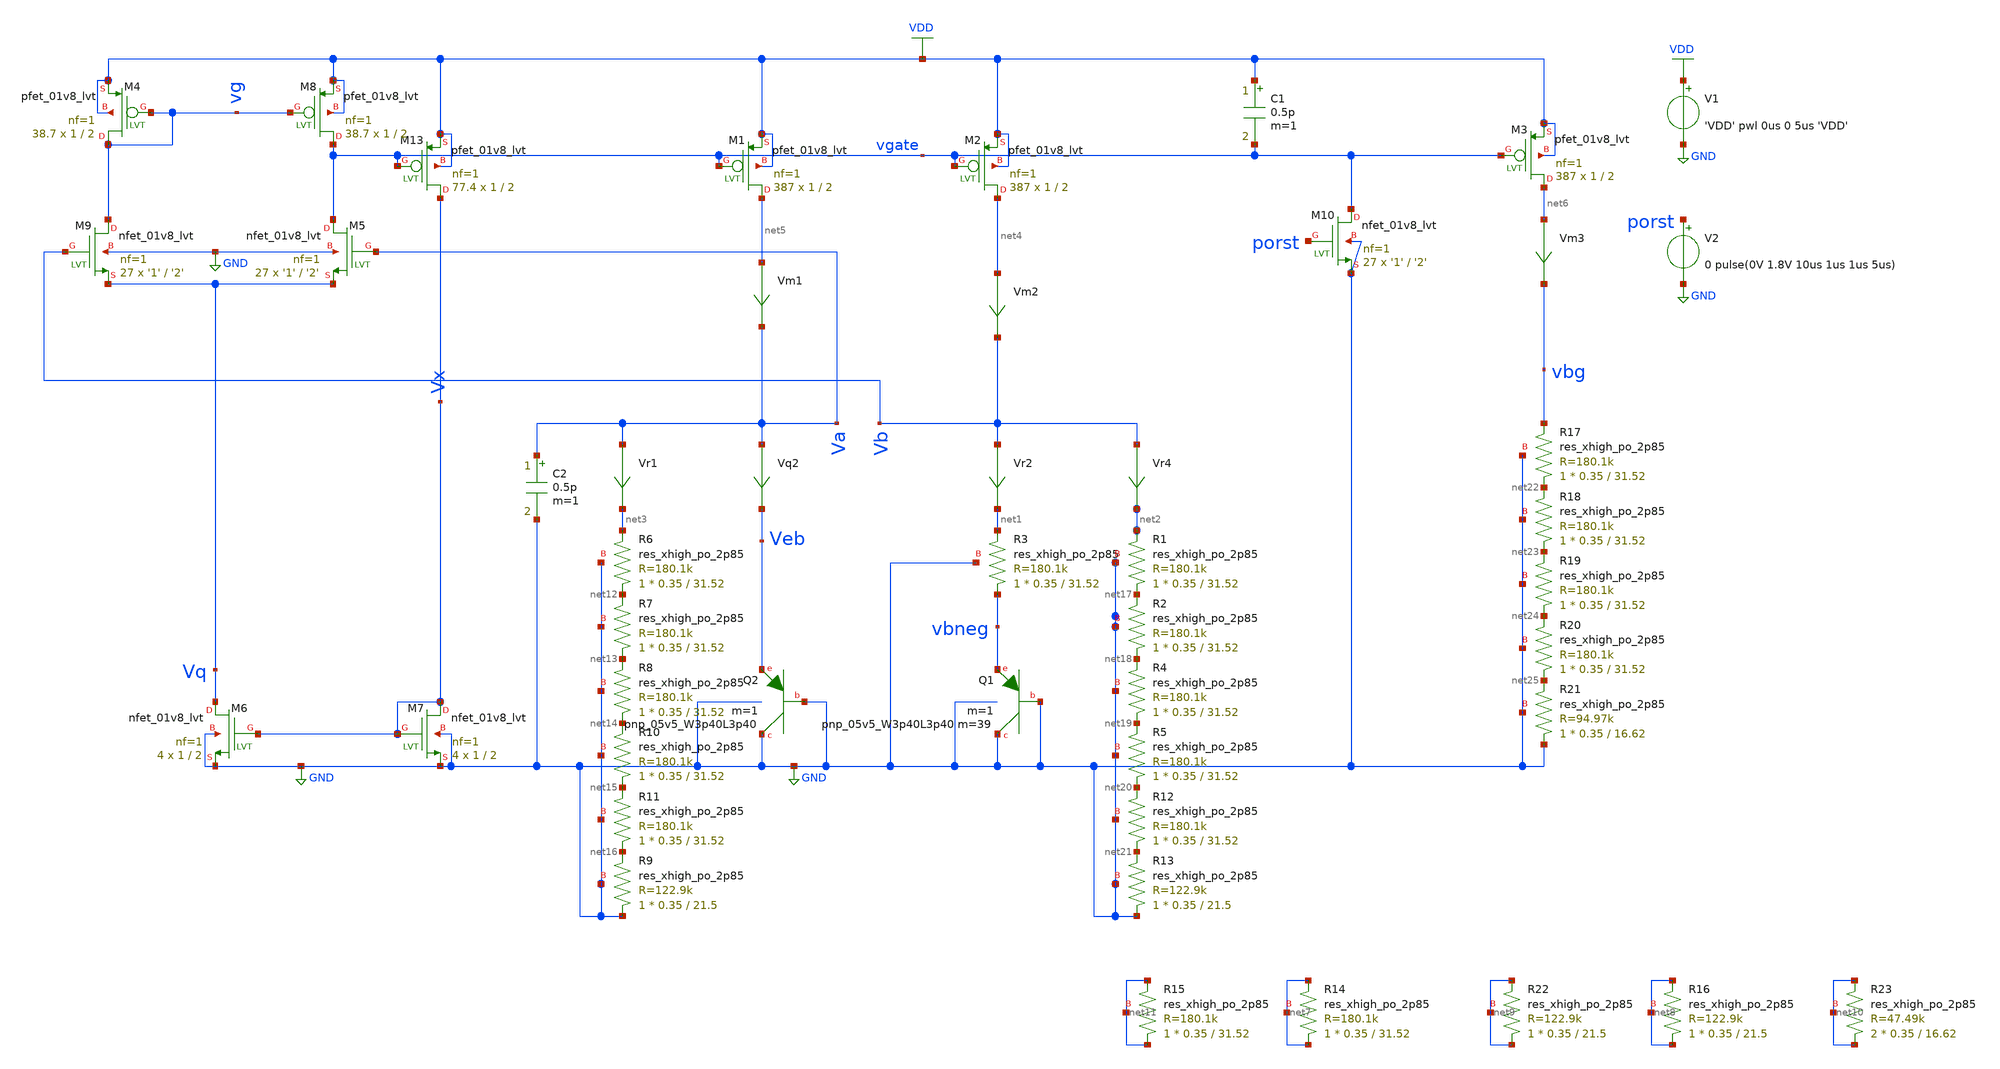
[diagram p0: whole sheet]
** sch_path: schematics/tsmc_bandgap_real_tran_layout.sch
**.subckt tsmc_bandgap_real_tran_layout
V1 VDD GND 'VDD' pwl 0us 0 5us 'VDD'
XQ2 GND GND Veb sky130_fd_pr__pnp_05v5_W3p40L3p40 m=1
Vr4 Vb net2 0
.save i(vr4)
Vr2 Vb net1 0
.save i(vr2)
Vm1 net5 Va 0
.save i(vm1)
Vm2 net4 Vb 0
.save i(vm2)
Vm3 net6 vbg 0
.save i(vm3)
Vr1 Va net3 0
.save i(vr1)
Vq2 Va Veb 0
.save i(vq2)
XQ1 GND GND vbneg sky130_fd_pr__pnp_05v5_W3p40L3p40 m=39 m=1
XM5 vgate Va Vq GND sky130_fd_pr__nfet_01v8_lvt L='2' W='1' nf=1 ad='int((nf+1)/2) * W/nf * 0.29' as='int((nf+2)/2) * W/nf * 0.29'
+ pd='2*int((nf+1)/2) * (W/nf + 0.29)' ps='2*int((nf+2)/2) * (W/nf + 0.29)' nrd='0.29 / W' nrs='0.29 / W'
+ sa=0 sb=0 sd=0 mult=27 m=27
XM6 Vq Vx GND GND sky130_fd_pr__nfet_01v8_lvt L=2 W=1 nf=1 ad='int((nf+1)/2) * W/nf * 0.29' as='int((nf+2)/2) * W/nf * 0.29'
+ pd='2*int((nf+1)/2) * (W/nf + 0.29)' ps='2*int((nf+2)/2) * (W/nf + 0.29)' nrd='0.29 / W' nrs='0.29 / W'
+ sa=0 sb=0 sd=0 mult=4 m=4
XM9 vg Vb Vq GND sky130_fd_pr__nfet_01v8_lvt L='2' W='1' nf=1 ad='int((nf+1)/2) * W/nf * 0.29' as='int((nf+2)/2) * W/nf * 0.29'
+ pd='2*int((nf+1)/2) * (W/nf + 0.29)' ps='2*int((nf+2)/2) * (W/nf + 0.29)' nrd='0.29 / W' nrs='0.29 / W'
+ sa=0 sb=0 sd=0 mult=27 m=27
XM7 Vx Vx GND GND sky130_fd_pr__nfet_01v8_lvt L=2 W=1 nf=1 ad='int((nf+1)/2) * W/nf * 0.29' as='int((nf+2)/2) * W/nf * 0.29'
+ pd='2*int((nf+1)/2) * (W/nf + 0.29)' ps='2*int((nf+2)/2) * (W/nf + 0.29)' nrd='0.29 / W' nrs='0.29 / W'
+ sa=0 sb=0 sd=0 mult=4 m=4
XM13 Vx vgate VDD VDD sky130_fd_pr__pfet_01v8_lvt L=2 W=1 nf=1 ad='int((nf+1)/2) * W/nf * 0.29' as='int((nf+2)/2) * W/nf * 0.29'
+ pd='2*int((nf+1)/2) * (W/nf + 0.29)' ps='2*int((nf+2)/2) * (W/nf + 0.29)' nrd='0.29 / W' nrs='0.29 / W'
+ sa=0 sb=0 sd=0 mult=77.4 m=77.4
XM1 net5 vgate VDD VDD sky130_fd_pr__pfet_01v8_lvt L=2 W=1 nf=1 ad='int((nf+1)/2) * W/nf * 0.29' as='int((nf+2)/2) * W/nf * 0.29'
+ pd='2*int((nf+1)/2) * (W/nf + 0.29)' ps='2*int((nf+2)/2) * (W/nf + 0.29)' nrd='0.29 / W' nrs='0.29 / W'
+ sa=0 sb=0 sd=0 mult=387 m=387
XM2 net4 vgate VDD VDD sky130_fd_pr__pfet_01v8_lvt L=2 W=1 nf=1 ad='int((nf+1)/2) * W/nf * 0.29' as='int((nf+2)/2) * W/nf * 0.29'
+ pd='2*int((nf+1)/2) * (W/nf + 0.29)' ps='2*int((nf+2)/2) * (W/nf + 0.29)' nrd='0.29 / W' nrs='0.29 / W'
+ sa=0 sb=0 sd=0 mult=387 m=387
XM3 net6 vgate VDD VDD sky130_fd_pr__pfet_01v8_lvt L=2 W=1 nf=1 ad='int((nf+1)/2) * W/nf * 0.29' as='int((nf+2)/2) * W/nf * 0.29'
+ pd='2*int((nf+1)/2) * (W/nf + 0.29)' ps='2*int((nf+2)/2) * (W/nf + 0.29)' nrd='0.29 / W' nrs='0.29 / W'
+ sa=0 sb=0 sd=0 mult=387 m=387
XM4 vg vg VDD VDD sky130_fd_pr__pfet_01v8_lvt L=2 W=1 nf=1 ad='int((nf+1)/2) * W/nf * 0.29' as='int((nf+2)/2) * W/nf * 0.29'
+ pd='2*int((nf+1)/2) * (W/nf + 0.29)' ps='2*int((nf+2)/2) * (W/nf + 0.29)' nrd='0.29 / W' nrs='0.29 / W'
+ sa=0 sb=0 sd=0 mult=38.7 m=38.7
XM8 vgate vg VDD VDD sky130_fd_pr__pfet_01v8_lvt L=2 W=1 nf=1 ad='int((nf+1)/2) * W/nf * 0.29' as='int((nf+2)/2) * W/nf * 0.29'
+ pd='2*int((nf+1)/2) * (W/nf + 0.29)' ps='2*int((nf+2)/2) * (W/nf + 0.29)' nrd='0.29 / W' nrs='0.29 / W'
+ sa=0 sb=0 sd=0 mult=38.7 m=38.7
XM10 vgate porst GND GND sky130_fd_pr__nfet_01v8_lvt L='2' W='1' nf=1 ad='int((nf+1)/2) * W/nf * 0.29'
+ as='int((nf+2)/2) * W/nf * 0.29' pd='2*int((nf+1)/2) * (W/nf + 0.29)' ps='2*int((nf+2)/2) * (W/nf + 0.29)'
+ nrd='0.29 / W' nrs='0.29 / W' sa=0 sb=0 sd=0 mult=27 m=27
V2 porst GND 0 pulse(0V 1.8V 10us 1us 1us 5us)
C1 VDD vgate 0.5p m=1
C2 Va GND 0.5p m=1
XR6 net12 net3 GND sky130_fd_pr__res_xhigh_po_2p85 L=31.52 mult=1 m=1
XR7 net13 net12 GND sky130_fd_pr__res_xhigh_po_2p85 L=31.52 mult=1 m=1
XR8 net14 net13 GND sky130_fd_pr__res_xhigh_po_2p85 L=31.52 mult=1 m=1
XR10 net15 net14 GND sky130_fd_pr__res_xhigh_po_2p85 L=31.52 mult=1 m=1
XR11 net16 net15 GND sky130_fd_pr__res_xhigh_po_2p85 L=31.52 mult=1 m=1
XR9 GND net16 GND sky130_fd_pr__res_xhigh_po_2p85 L=21.5 mult=1 m=1
XR3 vbneg net1 GND sky130_fd_pr__res_xhigh_po_2p85 L=31.52 mult=1 m=1
XR1 net17 net2 GND sky130_fd_pr__res_xhigh_po_2p85 L=31.52 mult=1 m=1
XR2 net18 net17 GND sky130_fd_pr__res_xhigh_po_2p85 L=31.52 mult=1 m=1
XR4 net19 net18 GND sky130_fd_pr__res_xhigh_po_2p85 L=31.52 mult=1 m=1
XR5 net20 net19 GND sky130_fd_pr__res_xhigh_po_2p85 L=31.52 mult=1 m=1
XR12 net21 net20 GND sky130_fd_pr__res_xhigh_po_2p85 L=31.52 mult=1 m=1
XR13 GND net21 GND sky130_fd_pr__res_xhigh_po_2p85 L=21.5 mult=1 m=1
XR17 net22 vbg GND sky130_fd_pr__res_xhigh_po_2p85 L=31.52 mult=1 m=1
XR18 net23 net22 GND sky130_fd_pr__res_xhigh_po_2p85 L=31.52 mult=1 m=1
XR19 net24 net23 GND sky130_fd_pr__res_xhigh_po_2p85 L=31.52 mult=1 m=1
XR20 net25 net24 GND sky130_fd_pr__res_xhigh_po_2p85 L=31.52 mult=1 m=1
XR21 GND net25 GND sky130_fd_pr__res_xhigh_po_2p85 L=16.62 mult=1 m=1
XR14 net7 net7 net7 sky130_fd_pr__res_xhigh_po_2p85 L=31.52 mult=1 m=1
XR15 net11 net11 net11 sky130_fd_pr__res_xhigh_po_2p85 L=31.52 mult=1 m=1
XR16 net8 net8 net8 sky130_fd_pr__res_xhigh_po_2p85 L=21.5 mult=1 m=1
XR22 net9 net9 net9 sky130_fd_pr__res_xhigh_po_2p85 L=21.5 mult=1 m=1
XR23 net10 net10 net10 sky130_fd_pr__res_xhigh_po_2p85 L=16.62 mult=2 m=2
**** begin user architecture code

.include $::SKYWATER_MODELS/cells/nfet_01v8/sky130_fd_pr__nfet_01v8__tt.corner.spice
.include $::SKYWATER_MODELS/cells/nfet_01v8_lvt/sky130_fd_pr__nfet_01v8_lvt__tt.corner.spice
.include $::SKYWATER_MODELS/cells/pfet_01v8/sky130_fd_pr__pfet_01v8__tt.corner.spice
.include $::SKYWATER_MODELS/cells/nfet_03v3_nvt/sky130_fd_pr__nfet_03v3_nvt__tt.corner.spice
.include $::SKYWATER_MODELS/cells/nfet_05v0_nvt/sky130_fd_pr__nfet_05v0_nvt__tt.corner.spice
.include $::SKYWATER_MODELS/cells/esd_nfet_01v8/sky130_fd_pr__esd_nfet_01v8__tt.corner.spice
.include $::SKYWATER_MODELS/cells/pfet_01v8_lvt/sky130_fd_pr__pfet_01v8_lvt__tt.corner.spice
.include $::SKYWATER_MODELS/cells/pfet_01v8_hvt/sky130_fd_pr__pfet_01v8_hvt__tt.corner.spice
.include $::SKYWATER_MODELS/cells/esd_pfet_g5v0d10v5/sky130_fd_pr__esd_pfet_g5v0d10v5__tt.corner.spice
.include $::SKYWATER_MODELS/cells/pfet_g5v0d10v5/sky130_fd_pr__pfet_g5v0d10v5__tt.corner.spice
.include $::SKYWATER_MODELS/cells/pfet_g5v0d16v0/sky130_fd_pr__pfet_g5v0d16v0__tt.corner.spice
.include $::SKYWATER_MODELS/cells/nfet_g5v0d10v5/sky130_fd_pr__nfet_g5v0d10v5__tt.corner.spice
.include $::SKYWATER_MODELS/cells/nfet_g5v0d16v0/sky130_fd_pr__nfet_g5v0d16v0__tt_discrete.corner.spice
.include $::SKYWATER_MODELS/cells/esd_nfet_g5v0d10v5/sky130_fd_pr__esd_nfet_g5v0d10v5__tt.corner.spice
.include $::SKYWATER_MODELS/models/corners/tt/nonfet.spice
* Mismatch parameters
.include $::SKYWATER_MODELS/cells/nfet_01v8/sky130_fd_pr__nfet_01v8__mismatch.corner.spice
.include $::SKYWATER_MODELS/cells/pfet_01v8/sky130_fd_pr__pfet_01v8__mismatch.corner.spice
.include $::SKYWATER_MODELS/cells/nfet_01v8_lvt/sky130_fd_pr__nfet_01v8_lvt__mismatch.corner.spice
.include $::SKYWATER_MODELS/cells/pfet_01v8_lvt/sky130_fd_pr__pfet_01v8_lvt__mismatch.corner.spice
.include $::SKYWATER_MODELS/cells/pfet_01v8_hvt/sky130_fd_pr__pfet_01v8_hvt__mismatch.corner.spice
.include $::SKYWATER_MODELS/cells/nfet_g5v0d10v5/sky130_fd_pr__nfet_g5v0d10v5__mismatch.corner.spice
.include $::SKYWATER_MODELS/cells/pfet_g5v0d10v5/sky130_fd_pr__pfet_g5v0d10v5__mismatch.corner.spice
.include $::SKYWATER_MODELS/cells/nfet_05v0_nvt/sky130_fd_pr__nfet_05v0_nvt__mismatch.corner.spice
.include $::SKYWATER_MODELS/cells/nfet_03v3_nvt/sky130_fd_pr__nfet_03v3_nvt__mismatch.corner.spice
* Resistor$::SKYWATER_MODELS/Capacitor
.include $::SKYWATER_MODELS/models/r+c/res_typical__cap_typical.spice
.include $::SKYWATER_MODELS/models/r+c/res_typical__cap_typical__lin.spice
* Special cells
.include $::SKYWATER_MODELS/models/corners/tt/specialized_cells.spice
* All models
.include $::SKYWATER_MODELS/models/all.spice
.include $::SKYWATER_MODELS/cells/pnp_05v5/sky130_fd_pr__pnp_05v5_W3p40L3p40.model.spice
* Corner
.include $::SKYWATER_MODELS/models/corners/tt/rf.spice



.option savecurrents
.param R3val='22.187k'
.param alpha='1'
.param R2R3ratio='5.6555038*alpha'
.param R2val='R3val*R2R3ratio'
.param R4R2ratio='0.79694273'
.param R4val='R2val*R4R2ratio
.param VDD=1.8
.control
save all  @m.xm1.msky130_fd_pr__pfet_01v8_lvt[gm]  @m.xm2.msky130_fd_pr__pfet_01v8_lvt[gm]  @m.xm3.msky130_fd_pr__pfet_01v8_lvt[gm]  @m.xm4.msky130_fd_pr__pfet_01v8_lvt[gm]  @m.xm5.msky130_fd_pr__nfet_01v8_lvt[gm]  @m.xm6.msky130_fd_pr__nfet_01v8_lvt[gm]  @m.xm7.msky130_fd_pr__nfet_01v8_lvt[gm]  @m.xm8.msky130_fd_pr__pfet_01v8_lvt[gm]  @m.xm9.msky130_fd_pr__nfet_01v8_lvt[gm]  @m.xm13.msky130_fd_pr__pfet_01v8_lvt[gm]

option temp=27
tran 0.1n 20u
option temp=0
tran 0.1n 20u
option temp=70
tran 0.1n 20u
write ./sims/tsmc_bandgap_real_layout_70degc_vbg.raw vbg
setplot tran2
write ./sims/tsmc_bandgap_real_layout_0degc_vbg.raw vbg
setplot tran1
write ./sims/tsmc_bandgap_real_layout_27degc_vbg.raw vbg
unset askquit
quit
.endc


**** end user architecture code
**.ends
.GLOBAL VDD
.GLOBAL GND
.end
